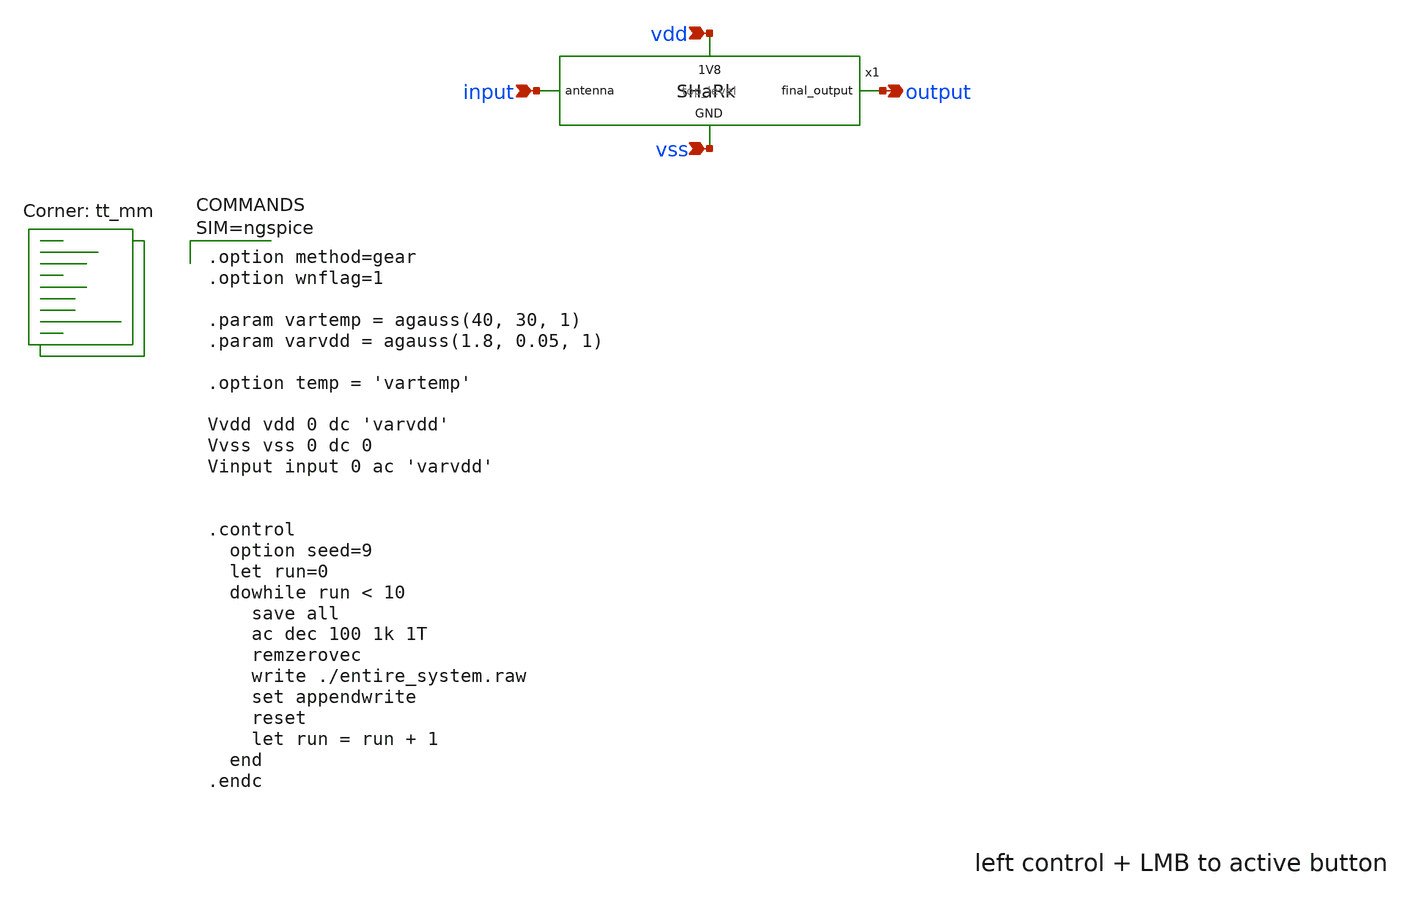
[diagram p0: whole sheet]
** sch_path: tests/entire_system.sch
**.subckt entire_system input output vdd vss
*.ipin input
*.opin output
*.ipin vdd
*.ipin vss
x1 vdd vss input output top_level
**** begin user architecture code
.lib $::SKYWATER_MODELS/sky130.lib.spice tt_mm


.option method=gear
.option wnflag=1

.param vartemp = agauss(40, 30, 1)
.param varvdd = agauss(1.8, 0.05, 1)

.option temp = 'vartemp'

Vvdd vdd 0 dc 'varvdd'
Vvss vss 0 dc 0
Vinput input 0 ac 'varvdd'


.control
  option seed=9
  let run=0
  dowhile run < 10
    save all
    ac dec 100 1k 1T
    remzerovec
    write ./entire_system.raw
    set appendwrite
    reset
    let run = run + 1
  end
.endc


**** end user architecture code
**.ends
.end
